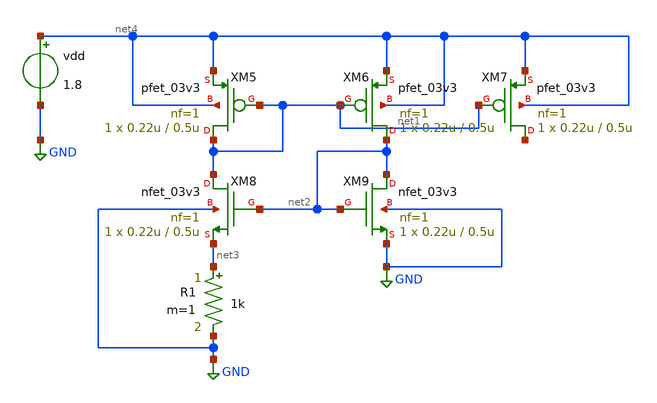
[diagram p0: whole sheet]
** sch_path: src/ChargePump/vdd_independent_ibias.sch
* Copyright 2022 GlobalFoundries PDK Authors
* Licensed under the Apache License, Version 2.0 (the "License");
* you may not use this file except in compliance with the License.
* You may obtain a copy of the License at
* https://www.apache.org/licenses/LICENSE-2.0
* Unless required by applicable law or agreed to in writing, software
* distributed under the License is distributed on an "AS IS" BASIS,
* WITHOUT WARRANTIES OR CONDITIONS OF ANY KIND, either express or implied.
* See the License for the specific language governing permissions and
* limitations under the License.
**.subckt vdd_independent_ibias
vdd net4 GND 1.8
XM5 net1 net1 net4 net4 pfet_03v3 L=0.5u W=0.22u nf=1 ad='int((nf+1)/2) * W/nf * 0.18u' as='int((nf+2)/2) * W/nf * 0.18u'
+ pd='2*int((nf+1)/2) * (W/nf + 0.18u)' ps='2*int((nf+2)/2) * (W/nf + 0.18u)' nrd='0.18u / W' nrs='0.18u / W'
+ sa=0 sb=0 sd=0 m=1
XM6 net2 net1 net4 net4 pfet_03v3 L=0.5u W=0.22u nf=1 ad='int((nf+1)/2) * W/nf * 0.18u' as='int((nf+2)/2) * W/nf * 0.18u'
+ pd='2*int((nf+1)/2) * (W/nf + 0.18u)' ps='2*int((nf+2)/2) * (W/nf + 0.18u)' nrd='0.18u / W' nrs='0.18u / W'
+ sa=0 sb=0 sd=0 m=1
XM7 net5 net1 net4 net4 pfet_03v3 L=0.5u W=0.22u nf=1 ad='int((nf+1)/2) * W/nf * 0.18u' as='int((nf+2)/2) * W/nf * 0.18u'
+ pd='2*int((nf+1)/2) * (W/nf + 0.18u)' ps='2*int((nf+2)/2) * (W/nf + 0.18u)' nrd='0.18u / W' nrs='0.18u / W'
+ sa=0 sb=0 sd=0 m=1
XM8 net1 net2 net3 GND nfet_03v3 L=0.5u W=0.22u nf=1 ad='int((nf+1)/2) * W/nf * 0.18u' as='int((nf+2)/2) * W/nf * 0.18u'
+ pd='2*int((nf+1)/2) * (W/nf + 0.18u)' ps='2*int((nf+2)/2) * (W/nf + 0.18u)' nrd='0.18u / W' nrs='0.18u / W'
+ sa=0 sb=0 sd=0 m=1
XM9 net2 net2 GND GND nfet_03v3 L=0.5u W=0.22u nf=1 ad='int((nf+1)/2) * W/nf * 0.18u' as='int((nf+2)/2) * W/nf * 0.18u'
+ pd='2*int((nf+1)/2) * (W/nf + 0.18u)' ps='2*int((nf+2)/2) * (W/nf + 0.18u)' nrd='0.18u / W' nrs='0.18u / W'
+ sa=0 sb=0 sd=0 m=1
R1 net3 GND 1k m=1
**.ends
.GLOBAL GND
.end
